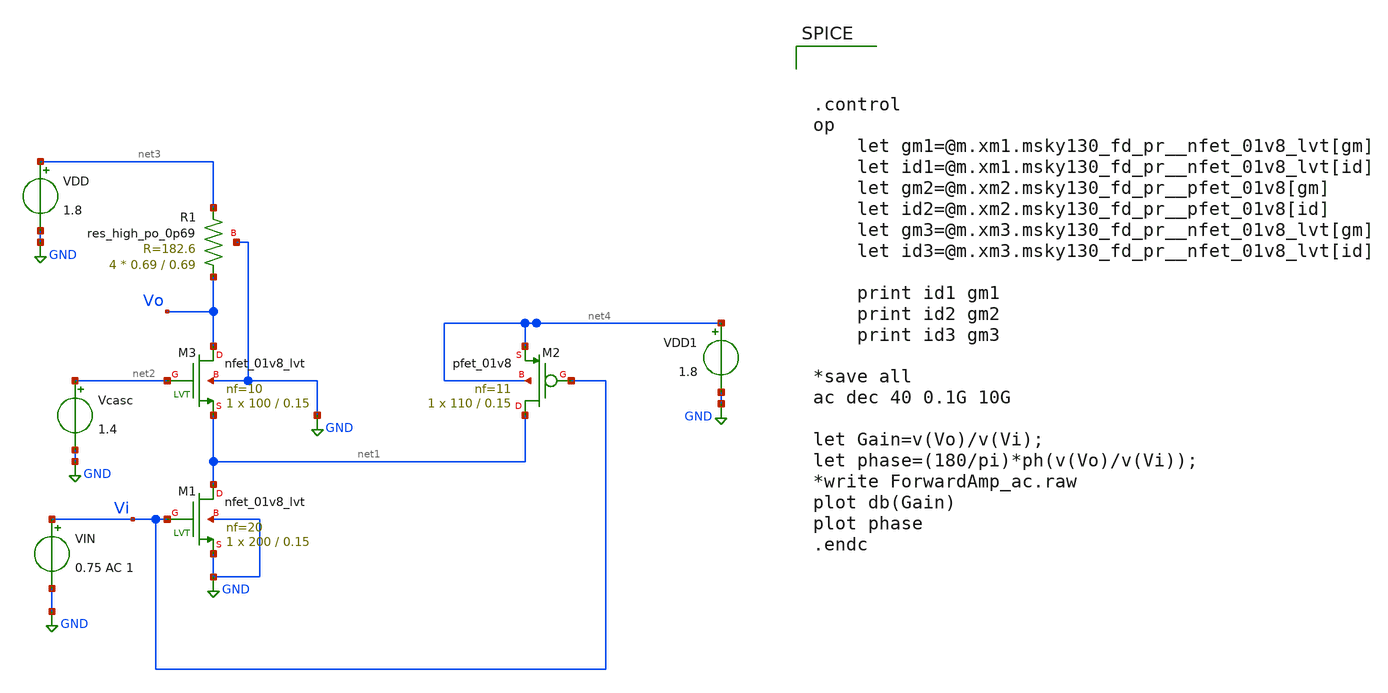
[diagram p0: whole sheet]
** sch_path: xschem/Forward_AMP.sch
**.subckt Forward_AMP
VIN Vi GND 0.75 AC 1
Vcasc net2 GND 1.4
VDD net3 GND 1.8
VDD1 net4 GND 1.8
XM1 net1 Vi GND GND sky130_fd_pr__nfet_01v8_lvt L=0.15 W=200 nf=20 ad='int((nf+1)/2) * W/nf * 0.29' as='int((nf+2)/2) * W/nf * 0.29'
+ pd='2*int((nf+1)/2) * (W/nf + 0.29)' ps='2*int((nf+2)/2) * (W/nf + 0.29)' nrd='0.29 / W' nrs='0.29 / W'
+ sa=0 sb=0 sd=0 mult=1 m=1
XM3 Vo net2 net1 GND sky130_fd_pr__nfet_01v8_lvt L=0.15 W=100 nf=10 ad='int((nf+1)/2) * W/nf * 0.29'
+ as='int((nf+2)/2) * W/nf * 0.29' pd='2*int((nf+1)/2) * (W/nf + 0.29)' ps='2*int((nf+2)/2) * (W/nf + 0.29)'
+ nrd='0.29 / W' nrs='0.29 / W' sa=0 sb=0 sd=0 mult=1 m=1
XM2 net1 Vi net4 net4 sky130_fd_pr__pfet_01v8 L=0.15 W=110 nf=11 ad='int((nf+1)/2) * W/nf * 0.29' as='int((nf+2)/2) * W/nf * 0.29'
+ pd='2*int((nf+1)/2) * (W/nf + 0.29)' ps='2*int((nf+2)/2) * (W/nf + 0.29)' nrd='0.29 / W' nrs='0.29 / W'
+ sa=0 sb=0 sd=0 mult=1 m=1
XR1 Vo net3 GND sky130_fd_pr__res_high_po_0p69 L=0.69 mult=4 m=4
**** begin user architecture code

.lib $::SKYWATER_MODELS/sky130.lib.spice tt




.control
op
	let gm1=@m.xm1.msky130_fd_pr__nfet_01v8_lvt[gm]
	let id1=@m.xm1.msky130_fd_pr__nfet_01v8_lvt[id]
	let gm2=@m.xm2.msky130_fd_pr__pfet_01v8[gm]
	let id2=@m.xm2.msky130_fd_pr__pfet_01v8[id]
	let gm3=@m.xm3.msky130_fd_pr__nfet_01v8_lvt[gm]
	let id3=@m.xm3.msky130_fd_pr__nfet_01v8_lvt[id]

	print id1 gm1
	print id2 gm2
	print id3 gm3

*save all
ac dec 40 0.1G 10G

let Gain=v(Vo)/v(Vi);
let phase=(180/pi)*ph(v(Vo)/v(Vi));
*write ForwardAmp_ac.raw
plot db(Gain)
plot phase
.endc


**** end user architecture code
**.ends
.GLOBAL GND
.end
